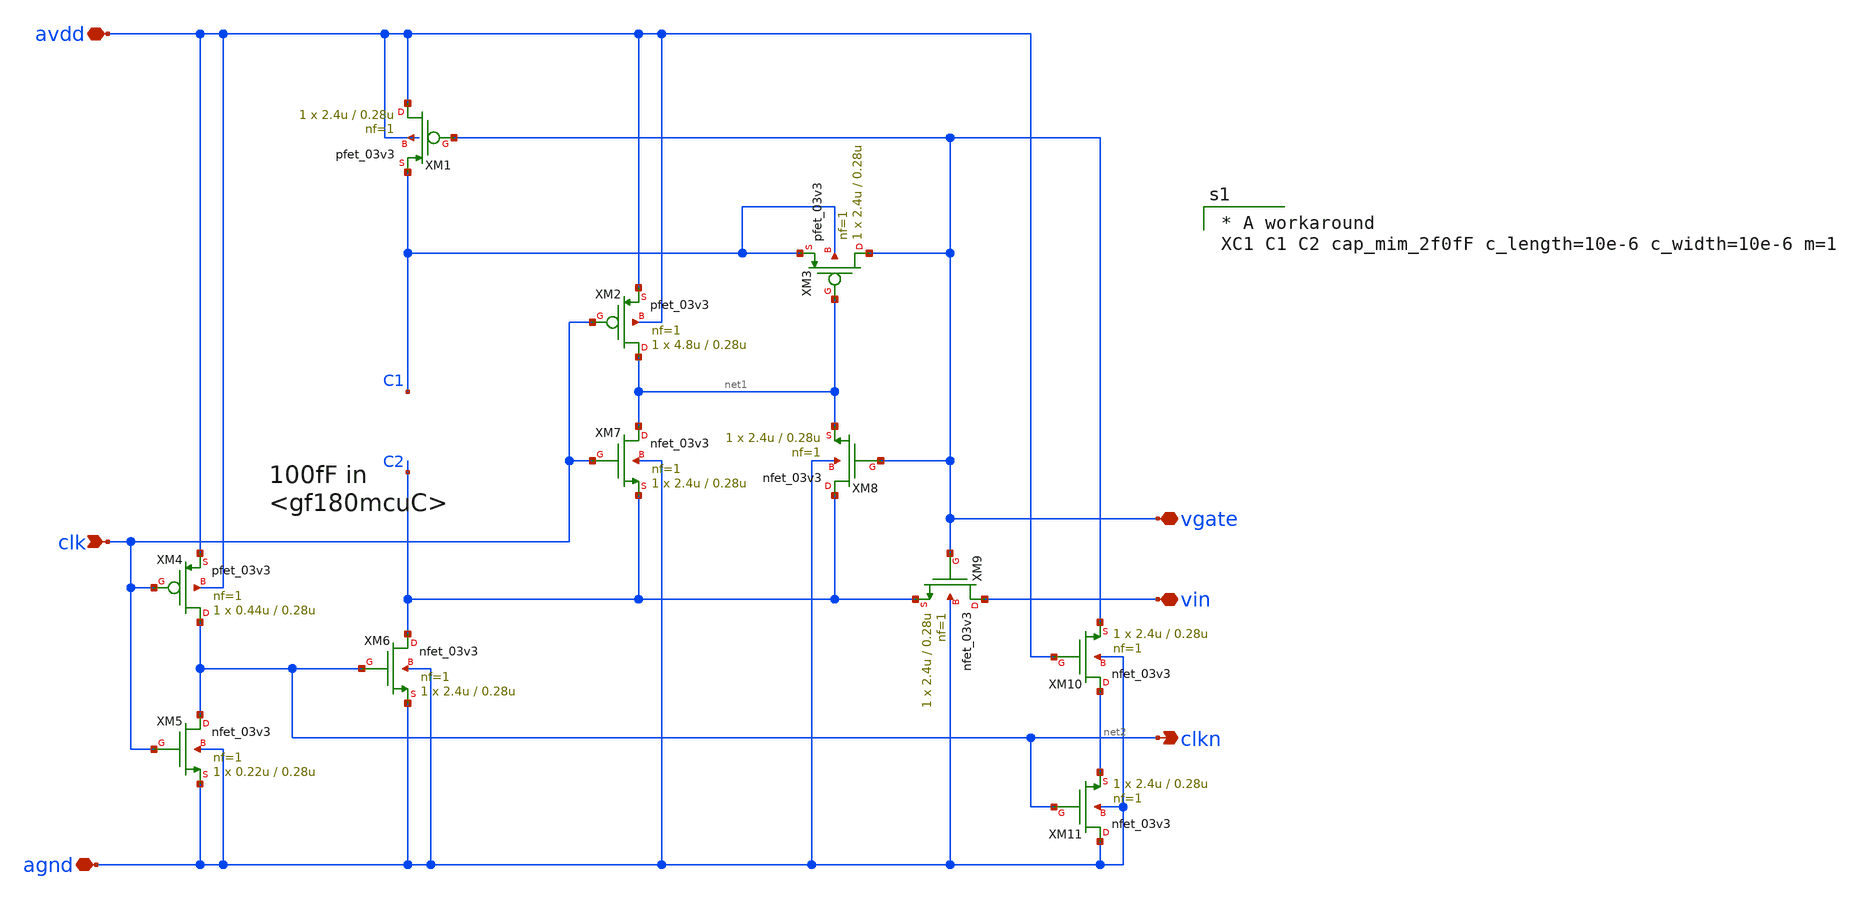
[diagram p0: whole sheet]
** sch_path: mpw18h1/cisar-gen/xschem/Bootstrapper.sch
**.subckt Bootstrapper avdd clk vgate agnd vin clkn
*.iopin avdd
*.ipin clk
*.iopin vgate
*.iopin agnd
*.iopin vin
*.opin clkn
XM1 avdd vgate C1 avdd pfet_03v3 L=0.28u W=2.4u nf=1 ad='int((nf+1)/2) * W/nf * 0.18u' as='int((nf+2)/2) * W/nf * 0.18u'
+ pd='2*int((nf+1)/2) * (W/nf + 0.18u)' ps='2*int((nf+2)/2) * (W/nf + 0.18u)' nrd='0.18u / W' nrs='0.18u / W'
+ sa=0 sb=0 sd=0 m=1 par=1
XM2 net1 clk avdd avdd pfet_03v3 L=0.28u W=4.8u nf=1 ad='int((nf+1)/2) * W/nf * 0.18u' as='int((nf+2)/2) * W/nf * 0.18u'
+ pd='2*int((nf+1)/2) * (W/nf + 0.18u)' ps='2*int((nf+2)/2) * (W/nf + 0.18u)' nrd='0.18u / W' nrs='0.18u / W'
+ sa=0 sb=0 sd=0 m=1 par=1
XM3 vgate net1 C1 C1 pfet_03v3 L=0.28u W=2.4u nf=1 ad='int((nf+1)/2) * W/nf * 0.18u' as='int((nf+2)/2) * W/nf * 0.18u'
+ pd='2*int((nf+1)/2) * (W/nf + 0.18u)' ps='2*int((nf+2)/2) * (W/nf + 0.18u)' nrd='0.18u / W' nrs='0.18u / W'
+ sa=0 sb=0 sd=0 m=1 par=1
XM4 clkn clk avdd avdd pfet_03v3 L=0.28u W=0.44u nf=1 ad='int((nf+1)/2) * W/nf * 0.18u' as='int((nf+2)/2) * W/nf * 0.18u'
+ pd='2*int((nf+1)/2) * (W/nf + 0.18u)' ps='2*int((nf+2)/2) * (W/nf + 0.18u)' nrd='0.18u / W' nrs='0.18u / W'
+ sa=0 sb=0 sd=0 m=1 par=1
XM5 clkn clk agnd agnd nfet_03v3 L=0.28u W=0.22u nf=1 ad='int((nf+1)/2) * W/nf * 0.18u' as='int((nf+2)/2) * W/nf * 0.18u'
+ pd='2*int((nf+1)/2) * (W/nf + 0.18u)' ps='2*int((nf+2)/2) * (W/nf + 0.18u)' nrd='0.18u / W' nrs='0.18u / W'
+ sa=0 sb=0 sd=0 m=1 par=1
XM6 C2 clkn agnd agnd nfet_03v3 L=0.28u W=2.4u nf=1 ad='int((nf+1)/2) * W/nf * 0.18u' as='int((nf+2)/2) * W/nf * 0.18u'
+ pd='2*int((nf+1)/2) * (W/nf + 0.18u)' ps='2*int((nf+2)/2) * (W/nf + 0.18u)' nrd='0.18u / W' nrs='0.18u / W'
+ sa=0 sb=0 sd=0 m=1 par=1
XM7 net1 clk C2 agnd nfet_03v3 L=0.28u W=2.4u nf=1 ad='int((nf+1)/2) * W/nf * 0.18u' as='int((nf+2)/2) * W/nf * 0.18u'
+ pd='2*int((nf+1)/2) * (W/nf + 0.18u)' ps='2*int((nf+2)/2) * (W/nf + 0.18u)' nrd='0.18u / W' nrs='0.18u / W'
+ sa=0 sb=0 sd=0 m=1 par=1
XM8 C2 vgate net1 agnd nfet_03v3 L=0.28u W=2.4u nf=1 ad='int((nf+1)/2) * W/nf * 0.18u' as='int((nf+2)/2) * W/nf * 0.18u'
+ pd='2*int((nf+1)/2) * (W/nf + 0.18u)' ps='2*int((nf+2)/2) * (W/nf + 0.18u)' nrd='0.18u / W' nrs='0.18u / W'
+ sa=0 sb=0 sd=0 m=1 par=1
XM9 vin vgate C2 agnd nfet_03v3 L=0.28u W=2.4u nf=1 ad='int((nf+1)/2) * W/nf * 0.18u' as='int((nf+2)/2) * W/nf * 0.18u'
+ pd='2*int((nf+1)/2) * (W/nf + 0.18u)' ps='2*int((nf+2)/2) * (W/nf + 0.18u)' nrd='0.18u / W' nrs='0.18u / W'
+ sa=0 sb=0 sd=0 m=1 par=1
XM10 net2 avdd vgate agnd nfet_03v3 L=0.28u W=2.4u nf=1 ad='int((nf+1)/2) * W/nf * 0.18u' as='int((nf+2)/2) * W/nf * 0.18u'
+ pd='2*int((nf+1)/2) * (W/nf + 0.18u)' ps='2*int((nf+2)/2) * (W/nf + 0.18u)' nrd='0.18u / W' nrs='0.18u / W'
+ sa=0 sb=0 sd=0 m=1 par=1
XM11 agnd clkn net2 agnd nfet_03v3 L=0.28u W=2.4u nf=1 ad='int((nf+1)/2) * W/nf * 0.18u' as='int((nf+2)/2) * W/nf * 0.18u'
+ pd='2*int((nf+1)/2) * (W/nf + 0.18u)' ps='2*int((nf+2)/2) * (W/nf + 0.18u)' nrd='0.18u / W' nrs='0.18u / W'
+ sa=0 sb=0 sd=0 m=1 par=1
**** begin user architecture code

* A workaround
XC1 C1 C2 cap_mim_2f0fF c_length=10e-6 c_width=10e-6 m=1


**** end user architecture code
**.ends
.end
